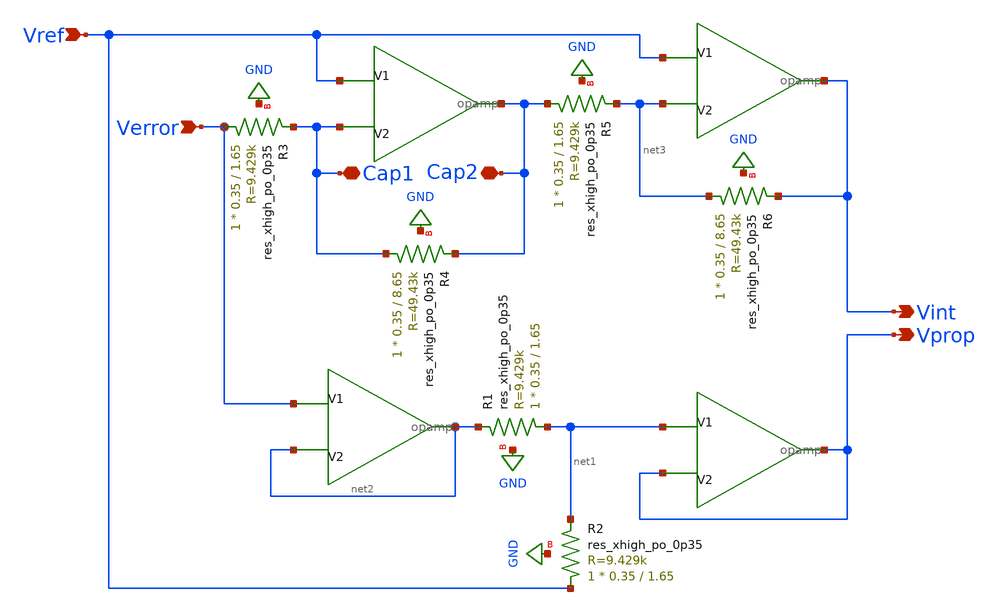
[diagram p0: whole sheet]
** sch_path: schematics/PI_controller.sch
**.subckt PI_controller Verror Vref Cap1 Cap2 Vint Vprop
*.ipin Verror
*.ipin Vref
*.iopin Cap1
*.iopin Cap2
*.opin Vint
*.opin Vprop
X3 Verror net2 net2 opamp
XR1 net1 net2 GND sky130_fd_pr__res_xhigh_po_0p35 L=1.65 mult=1 m=1
X1 net1 Vprop Vprop opamp
XR2 Vref net1 GND sky130_fd_pr__res_xhigh_po_0p35 L=1.65 mult=1 m=1
X2 Vref Cap1 Cap2 opamp
X4 Vref net3 Vint opamp
XR3 Verror Cap1 GND sky130_fd_pr__res_xhigh_po_0p35 L=1.65 mult=1 m=1
XR4 Cap1 Cap2 GND sky130_fd_pr__res_xhigh_po_0p35 L=8.65 mult=1 m=1
XR5 Cap2 net3 GND sky130_fd_pr__res_xhigh_po_0p35 L=1.65 mult=1 m=1
XR6 net3 Vint GND sky130_fd_pr__res_xhigh_po_0p35 L=8.65 mult=1 m=1
**.ends

* expanding   symbol:  /home/madvlsi/Documents/MADVLSI_final/schematics/opamp.sym # of pins=3
** sym_path: schematics/opamp.sym
** sch_path: schematics/opamp.sch
.subckt opamp V1 V2 VOUT
*.ipin V1
*.ipin V2
*.opin VOUT
XM19 net12 net10 GND VDD sky130_fd_pr__pfet_01v8 L=.6 W=1.5 nf=1 ad='int((nf+1)/2) * W/nf * 0.29' as='int((nf+2)/2) * W/nf * 0.29'
+ pd='2*int((nf+1)/2) * (W/nf + 0.29)' ps='2*int((nf+2)/2) * (W/nf + 0.29)' nrd='0.29 / W' nrs='0.29 / W'
+ sa=0 sb=0 sd=0 mult=1 m=1
XMD20 VDD VDD net12 VDD sky130_fd_pr__pfet_01v8 L=.6 W=1.5 nf=1 ad='int((nf+1)/2) * W/nf * 0.29' as='int((nf+2)/2) * W/nf * 0.29'
+ pd='2*int((nf+1)/2) * (W/nf + 0.29)' ps='2*int((nf+2)/2) * (W/nf + 0.29)' nrd='0.29 / W' nrs='0.29 / W'
+ sa=0 sb=0 sd=0 mult=1 m=1
XM22 net12 net10 net9 VDD sky130_fd_pr__pfet_01v8 L=.6 W=1.5 nf=1 ad='int((nf+1)/2) * W/nf * 0.29' as='int((nf+2)/2) * W/nf * 0.29'
+ pd='2*int((nf+1)/2) * (W/nf + 0.29)' ps='2*int((nf+2)/2) * (W/nf + 0.29)' nrd='0.29 / W' nrs='0.29 / W'
+ sa=0 sb=0 sd=0 mult=1 m=1
XM23 GND net10 net12 VDD sky130_fd_pr__pfet_01v8 L=.6 W=1.5 nf=1 ad='int((nf+1)/2) * W/nf * 0.29' as='int((nf+2)/2) * W/nf * 0.29'
+ pd='2*int((nf+1)/2) * (W/nf + 0.29)' ps='2*int((nf+2)/2) * (W/nf + 0.29)' nrd='0.29 / W' nrs='0.29 / W'
+ sa=0 sb=0 sd=0 mult=1 m=1
XMD24 net9 VDD net10 VDD sky130_fd_pr__pfet_01v8 L=.6 W=1.5 nf=1 ad='int((nf+1)/2) * W/nf * 0.29' as='int((nf+2)/2) * W/nf * 0.29'
+ pd='2*int((nf+1)/2) * (W/nf + 0.29)' ps='2*int((nf+2)/2) * (W/nf + 0.29)' nrd='0.29 / W' nrs='0.29 / W'
+ sa=0 sb=0 sd=0 mult=1 m=1
XM25 VDD net10 net12 VDD sky130_fd_pr__pfet_01v8 L=.6 W=1.5 nf=1 ad='int((nf+1)/2) * W/nf * 0.29' as='int((nf+2)/2) * W/nf * 0.29'
+ pd='2*int((nf+1)/2) * (W/nf + 0.29)' ps='2*int((nf+2)/2) * (W/nf + 0.29)' nrd='0.29 / W' nrs='0.29 / W'
+ sa=0 sb=0 sd=0 mult=1 m=1
XM26 net7 V2 net11 VDD sky130_fd_pr__pfet_01v8 L=.6 W=1.5 nf=1 ad='int((nf+1)/2) * W/nf * 0.29' as='int((nf+2)/2) * W/nf * 0.29'
+ pd='2*int((nf+1)/2) * (W/nf + 0.29)' ps='2*int((nf+2)/2) * (W/nf + 0.29)' nrd='0.29 / W' nrs='0.29 / W'
+ sa=0 sb=0 sd=0 mult=1 m=1
XMD27 net5 VDD net14 VDD sky130_fd_pr__pfet_01v8 L=.6 W=1.5 nf=1 ad='int((nf+1)/2) * W/nf * 0.29' as='int((nf+2)/2) * W/nf * 0.29'
+ pd='2*int((nf+1)/2) * (W/nf + 0.29)' ps='2*int((nf+2)/2) * (W/nf + 0.29)' nrd='0.29 / W' nrs='0.29 / W'
+ sa=0 sb=0 sd=0 mult=1 m=1
XM28 net6 V1 net11 VDD sky130_fd_pr__pfet_01v8 L=.6 W=1.5 nf=1 ad='int((nf+1)/2) * W/nf * 0.29' as='int((nf+2)/2) * W/nf * 0.29'
+ pd='2*int((nf+1)/2) * (W/nf + 0.29)' ps='2*int((nf+2)/2) * (W/nf + 0.29)' nrd='0.29 / W' nrs='0.29 / W'
+ sa=0 sb=0 sd=0 mult=1 m=1
XM29 net11 net10 VDD VDD sky130_fd_pr__pfet_01v8 L=.6 W=1.5 nf=1 ad='int((nf+1)/2) * W/nf * 0.29' as='int((nf+2)/2) * W/nf * 0.29'
+ pd='2*int((nf+1)/2) * (W/nf + 0.29)' ps='2*int((nf+2)/2) * (W/nf + 0.29)' nrd='0.29 / W' nrs='0.29 / W'
+ sa=0 sb=0 sd=0 mult=1 m=1
XMD30 net11 VDD VDD VDD sky130_fd_pr__pfet_01v8 L=.6 W=1.5 nf=1 ad='int((nf+1)/2) * W/nf * 0.29' as='int((nf+2)/2) * W/nf * 0.29'
+ pd='2*int((nf+1)/2) * (W/nf + 0.29)' ps='2*int((nf+2)/2) * (W/nf + 0.29)' nrd='0.29 / W' nrs='0.29 / W'
+ sa=0 sb=0 sd=0 mult=1 m=1
XMD31 net2 VDD net13 VDD sky130_fd_pr__pfet_01v8 L=.6 W=1.5 nf=1 ad='int((nf+1)/2) * W/nf * 0.29' as='int((nf+2)/2) * W/nf * 0.29'
+ pd='2*int((nf+1)/2) * (W/nf + 0.29)' ps='2*int((nf+2)/2) * (W/nf + 0.29)' nrd='0.29 / W' nrs='0.29 / W'
+ sa=0 sb=0 sd=0 mult=1 m=1
XM32 net4 net5 net5 VDD sky130_fd_pr__pfet_01v8 L=.6 W=1.5 nf=1 ad='int((nf+1)/2) * W/nf * 0.29' as='int((nf+2)/2) * W/nf * 0.29'
+ pd='2*int((nf+1)/2) * (W/nf + 0.29)' ps='2*int((nf+2)/2) * (W/nf + 0.29)' nrd='0.29 / W' nrs='0.29 / W'
+ sa=0 sb=0 sd=0 mult=1 m=1
XM33 VDD net10 net4 VDD sky130_fd_pr__pfet_01v8 L=.6 W=1.5 nf=1 ad='int((nf+1)/2) * W/nf * 0.29' as='int((nf+2)/2) * W/nf * 0.29'
+ pd='2*int((nf+1)/2) * (W/nf + 0.29)' ps='2*int((nf+2)/2) * (W/nf + 0.29)' nrd='0.29 / W' nrs='0.29 / W'
+ sa=0 sb=0 sd=0 mult=1 m=1
XM34 net3 net5 net2 VDD sky130_fd_pr__pfet_01v8 L=.6 W=1.5 nf=1 ad='int((nf+1)/2) * W/nf * 0.29' as='int((nf+2)/2) * W/nf * 0.29'
+ pd='2*int((nf+1)/2) * (W/nf + 0.29)' ps='2*int((nf+2)/2) * (W/nf + 0.29)' nrd='0.29 / W' nrs='0.29 / W'
+ sa=0 sb=0 sd=0 mult=1 m=1
XM35 VDD net10 net3 VDD sky130_fd_pr__pfet_01v8 L=.6 W=1.5 nf=1 ad='int((nf+1)/2) * W/nf * 0.29' as='int((nf+2)/2) * W/nf * 0.29'
+ pd='2*int((nf+1)/2) * (W/nf + 0.29)' ps='2*int((nf+2)/2) * (W/nf + 0.29)' nrd='0.29 / W' nrs='0.29 / W'
+ sa=0 sb=0 sd=0 mult=1 m=1
XM36 VOUT net2 VDD VDD sky130_fd_pr__pfet_01v8 L=.6 W=1.5 nf=1 ad='int((nf+1)/2) * W/nf * 0.29' as='int((nf+2)/2) * W/nf * 0.29'
+ pd='2*int((nf+1)/2) * (W/nf + 0.29)' ps='2*int((nf+2)/2) * (W/nf + 0.29)' nrd='0.29 / W' nrs='0.29 / W'
+ sa=0 sb=0 sd=0 mult=1 m=1
XM37 VDD net2 VOUT VDD sky130_fd_pr__pfet_01v8 L=.6 W=1.5 nf=1 ad='int((nf+1)/2) * W/nf * 0.29' as='int((nf+2)/2) * W/nf * 0.29'
+ pd='2*int((nf+1)/2) * (W/nf + 0.29)' ps='2*int((nf+2)/2) * (W/nf + 0.29)' nrd='0.29 / W' nrs='0.29 / W'
+ sa=0 sb=0 sd=0 mult=1 m=1
XM38 VOUT net2 VDD VDD sky130_fd_pr__pfet_01v8 L=.6 W=1.5 nf=1 ad='int((nf+1)/2) * W/nf * 0.29' as='int((nf+2)/2) * W/nf * 0.29'
+ pd='2*int((nf+1)/2) * (W/nf + 0.29)' ps='2*int((nf+2)/2) * (W/nf + 0.29)' nrd='0.29 / W' nrs='0.29 / W'
+ sa=0 sb=0 sd=0 mult=1 m=1
XM39 VDD net2 VOUT VDD sky130_fd_pr__pfet_01v8 L=.6 W=1.5 nf=1 ad='int((nf+1)/2) * W/nf * 0.29' as='int((nf+2)/2) * W/nf * 0.29'
+ pd='2*int((nf+1)/2) * (W/nf + 0.29)' ps='2*int((nf+2)/2) * (W/nf + 0.29)' nrd='0.29 / W' nrs='0.29 / W'
+ sa=0 sb=0 sd=0 mult=1 m=1
XM40 net1 net9 VDD GND sky130_fd_pr__nfet_01v8 L=.6 W=1.5 nf=1 ad='int((nf+1)/2) * W/nf * 0.29' as='int((nf+2)/2) * W/nf * 0.29'
+ pd='2*int((nf+1)/2) * (W/nf + 0.29)' ps='2*int((nf+2)/2) * (W/nf + 0.29)' nrd='0.29 / W' nrs='0.29 / W'
+ sa=0 sb=0 sd=0 mult=1 m=1
XMD41 GND GND net1 GND sky130_fd_pr__nfet_01v8 L=.6 W=1.5 nf=1 ad='int((nf+1)/2) * W/nf * 0.29' as='int((nf+2)/2) * W/nf * 0.29'
+ pd='2*int((nf+1)/2) * (W/nf + 0.29)' ps='2*int((nf+2)/2) * (W/nf + 0.29)' nrd='0.29 / W' nrs='0.29 / W'
+ sa=0 sb=0 sd=0 mult=1 m=1
XM42 net1 net9 net10 GND sky130_fd_pr__nfet_01v8 L=.6 W=1.5 nf=1 ad='int((nf+1)/2) * W/nf * 0.29' as='int((nf+2)/2) * W/nf * 0.29'
+ pd='2*int((nf+1)/2) * (W/nf + 0.29)' ps='2*int((nf+2)/2) * (W/nf + 0.29)' nrd='0.29 / W' nrs='0.29 / W'
+ sa=0 sb=0 sd=0 mult=1 m=1
XM43 VDD net9 net1 GND sky130_fd_pr__nfet_01v8 L=.6 W=1.5 nf=1 ad='int((nf+1)/2) * W/nf * 0.29' as='int((nf+2)/2) * W/nf * 0.29'
+ pd='2*int((nf+1)/2) * (W/nf + 0.29)' ps='2*int((nf+2)/2) * (W/nf + 0.29)' nrd='0.29 / W' nrs='0.29 / W'
+ sa=0 sb=0 sd=0 mult=1 m=1
XMD44 net10 GND net9 GND sky130_fd_pr__nfet_01v8 L=.6 W=1.5 nf=1 ad='int((nf+1)/2) * W/nf * 0.29' as='int((nf+2)/2) * W/nf * 0.29'
+ pd='2*int((nf+1)/2) * (W/nf + 0.29)' ps='2*int((nf+2)/2) * (W/nf + 0.29)' nrd='0.29 / W' nrs='0.29 / W'
+ sa=0 sb=0 sd=0 mult=1 m=1
XM45 GND net9 net1 GND sky130_fd_pr__nfet_01v8 L=.6 W=1.5 nf=1 ad='int((nf+1)/2) * W/nf * 0.29' as='int((nf+2)/2) * W/nf * 0.29'
+ pd='2*int((nf+1)/2) * (W/nf + 0.29)' ps='2*int((nf+2)/2) * (W/nf + 0.29)' nrd='0.29 / W' nrs='0.29 / W'
+ sa=0 sb=0 sd=0 mult=1 m=1
XM46 net3 V1 net8 GND sky130_fd_pr__nfet_01v8 L=.6 W=1.5 nf=1 ad='int((nf+1)/2) * W/nf * 0.29' as='int((nf+2)/2) * W/nf * 0.29'
+ pd='2*int((nf+1)/2) * (W/nf + 0.29)' ps='2*int((nf+2)/2) * (W/nf + 0.29)' nrd='0.29 / W' nrs='0.29 / W'
+ sa=0 sb=0 sd=0 mult=1 m=1
XMD47 net5 GND net15 GND sky130_fd_pr__nfet_01v8 L=.6 W=1.5 nf=1 ad='int((nf+1)/2) * W/nf * 0.29' as='int((nf+2)/2) * W/nf * 0.29'
+ pd='2*int((nf+1)/2) * (W/nf + 0.29)' ps='2*int((nf+2)/2) * (W/nf + 0.29)' nrd='0.29 / W' nrs='0.29 / W'
+ sa=0 sb=0 sd=0 mult=1 m=1
XM48 net4 V2 net8 GND sky130_fd_pr__nfet_01v8 L=.6 W=1.5 nf=1 ad='int((nf+1)/2) * W/nf * 0.29' as='int((nf+2)/2) * W/nf * 0.29'
+ pd='2*int((nf+1)/2) * (W/nf + 0.29)' ps='2*int((nf+2)/2) * (W/nf + 0.29)' nrd='0.29 / W' nrs='0.29 / W'
+ sa=0 sb=0 sd=0 mult=1 m=1
XM49 net8 net9 GND GND sky130_fd_pr__nfet_01v8 L=.6 W=1.5 nf=1 ad='int((nf+1)/2) * W/nf * 0.29' as='int((nf+2)/2) * W/nf * 0.29'
+ pd='2*int((nf+1)/2) * (W/nf + 0.29)' ps='2*int((nf+2)/2) * (W/nf + 0.29)' nrd='0.29 / W' nrs='0.29 / W'
+ sa=0 sb=0 sd=0 mult=1 m=1
XMD50 net8 GND GND GND sky130_fd_pr__nfet_01v8 L=.6 W=1.5 nf=1 ad='int((nf+1)/2) * W/nf * 0.29' as='int((nf+2)/2) * W/nf * 0.29'
+ pd='2*int((nf+1)/2) * (W/nf + 0.29)' ps='2*int((nf+2)/2) * (W/nf + 0.29)' nrd='0.29 / W' nrs='0.29 / W'
+ sa=0 sb=0 sd=0 mult=1 m=1
XMD51 net2 GND net16 GND sky130_fd_pr__nfet_01v8 L=.6 W=1.5 nf=1 ad='int((nf+1)/2) * W/nf * 0.29' as='int((nf+2)/2) * W/nf * 0.29'
+ pd='2*int((nf+1)/2) * (W/nf + 0.29)' ps='2*int((nf+2)/2) * (W/nf + 0.29)' nrd='0.29 / W' nrs='0.29 / W'
+ sa=0 sb=0 sd=0 mult=1 m=1
XM52 GND net9 net7 GND sky130_fd_pr__nfet_01v8 L=.6 W=1.5 nf=1 ad='int((nf+1)/2) * W/nf * 0.29' as='int((nf+2)/2) * W/nf * 0.29'
+ pd='2*int((nf+1)/2) * (W/nf + 0.29)' ps='2*int((nf+2)/2) * (W/nf + 0.29)' nrd='0.29 / W' nrs='0.29 / W'
+ sa=0 sb=0 sd=0 mult=1 m=1
XMD53 VOUT GND GND GND sky130_fd_pr__nfet_01v8 L=.6 W=1.5 nf=1 ad='int((nf+1)/2) * W/nf * 0.29' as='int((nf+2)/2) * W/nf * 0.29'
+ pd='2*int((nf+1)/2) * (W/nf + 0.29)' ps='2*int((nf+2)/2) * (W/nf + 0.29)' nrd='0.29 / W' nrs='0.29 / W'
+ sa=0 sb=0 sd=0 mult=1 m=1
XM54 GND net9 net6 GND sky130_fd_pr__nfet_01v8 L=.6 W=1.5 nf=1 ad='int((nf+1)/2) * W/nf * 0.29' as='int((nf+2)/2) * W/nf * 0.29'
+ pd='2*int((nf+1)/2) * (W/nf + 0.29)' ps='2*int((nf+2)/2) * (W/nf + 0.29)' nrd='0.29 / W' nrs='0.29 / W'
+ sa=0 sb=0 sd=0 mult=1 m=1
XM55 net7 net5 net5 GND sky130_fd_pr__nfet_01v8 L=.6 W=1.5 nf=1 ad='int((nf+1)/2) * W/nf * 0.29' as='int((nf+2)/2) * W/nf * 0.29'
+ pd='2*int((nf+1)/2) * (W/nf + 0.29)' ps='2*int((nf+2)/2) * (W/nf + 0.29)' nrd='0.29 / W' nrs='0.29 / W'
+ sa=0 sb=0 sd=0 mult=1 m=1
XM56 net6 net5 net2 GND sky130_fd_pr__nfet_01v8 L=.6 W=1.5 nf=1 ad='int((nf+1)/2) * W/nf * 0.29' as='int((nf+2)/2) * W/nf * 0.29'
+ pd='2*int((nf+1)/2) * (W/nf + 0.29)' ps='2*int((nf+2)/2) * (W/nf + 0.29)' nrd='0.29 / W' nrs='0.29 / W'
+ sa=0 sb=0 sd=0 mult=1 m=1
XMD57 VOUT GND GND GND sky130_fd_pr__nfet_01v8 L=.6 W=1.5 nf=1 ad='int((nf+1)/2) * W/nf * 0.29' as='int((nf+2)/2) * W/nf * 0.29'
+ pd='2*int((nf+1)/2) * (W/nf + 0.29)' ps='2*int((nf+2)/2) * (W/nf + 0.29)' nrd='0.29 / W' nrs='0.29 / W'
+ sa=0 sb=0 sd=0 mult=1 m=1
XM58 GND net2 VOUT GND sky130_fd_pr__nfet_01v8 L=.6 W=1.5 nf=1 ad='int((nf+1)/2) * W/nf * 0.29' as='int((nf+2)/2) * W/nf * 0.29'
+ pd='2*int((nf+1)/2) * (W/nf + 0.29)' ps='2*int((nf+2)/2) * (W/nf + 0.29)' nrd='0.29 / W' nrs='0.29 / W'
+ sa=0 sb=0 sd=0 mult=1 m=1
XM59 GND net2 VOUT GND sky130_fd_pr__nfet_01v8 L=.6 W=1.5 nf=1 ad='int((nf+1)/2) * W/nf * 0.29' as='int((nf+2)/2) * W/nf * 0.29'
+ pd='2*int((nf+1)/2) * (W/nf + 0.29)' ps='2*int((nf+2)/2) * (W/nf + 0.29)' nrd='0.29 / W' nrs='0.29 / W'
+ sa=0 sb=0 sd=0 mult=1 m=1
XM60 net12 net10 GND VDD sky130_fd_pr__pfet_01v8 L=.6 W=1.5 nf=1 ad='int((nf+1)/2) * W/nf * 0.29' as='int((nf+2)/2) * W/nf * 0.29'
+ pd='2*int((nf+1)/2) * (W/nf + 0.29)' ps='2*int((nf+2)/2) * (W/nf + 0.29)' nrd='0.29 / W' nrs='0.29 / W'
+ sa=0 sb=0 sd=0 mult=1 m=1
XM61 net10 net10 net4 VDD sky130_fd_pr__pfet_01v8 L=.6 W=1.5 nf=1 ad='int((nf+1)/2) * W/nf * 0.29' as='int((nf+2)/2) * W/nf * 0.29'
+ pd='2*int((nf+1)/2) * (W/nf + 0.29)' ps='2*int((nf+2)/2) * (W/nf + 0.29)' nrd='0.29 / W' nrs='0.29 / W'
+ sa=0 sb=0 sd=0 mult=1 m=1
XM62 net1 net9 VDD GND sky130_fd_pr__nfet_01v8 L=.6 W=1.5 nf=1 ad='int((nf+1)/2) * W/nf * 0.29' as='int((nf+2)/2) * W/nf * 0.29'
+ pd='2*int((nf+1)/2) * (W/nf + 0.29)' ps='2*int((nf+2)/2) * (W/nf + 0.29)' nrd='0.29 / W' nrs='0.29 / W'
+ sa=0 sb=0 sd=0 mult=1 m=1
XM63 net9 net9 net7 GND sky130_fd_pr__nfet_01v8 L=.6 W=1.5 nf=1 ad='int((nf+1)/2) * W/nf * 0.29' as='int((nf+2)/2) * W/nf * 0.29'
+ pd='2*int((nf+1)/2) * (W/nf + 0.29)' ps='2*int((nf+2)/2) * (W/nf + 0.29)' nrd='0.29 / W' nrs='0.29 / W'
+ sa=0 sb=0 sd=0 mult=1 m=1
XMD64 VDD GND GND GND sky130_fd_pr__nfet_01v8 L=.6 W=1.5 nf=1 ad='int((nf+1)/2) * W/nf * 0.29' as='int((nf+2)/2) * W/nf * 0.29'
+ pd='2*int((nf+1)/2) * (W/nf + 0.29)' ps='2*int((nf+2)/2) * (W/nf + 0.29)' nrd='0.29 / W' nrs='0.29 / W'
+ sa=0 sb=0 sd=0 mult=1 m=1
XMD65 net7 GND GND GND sky130_fd_pr__nfet_01v8 L=.6 W=1.5 nf=1 ad='int((nf+1)/2) * W/nf * 0.29' as='int((nf+2)/2) * W/nf * 0.29'
+ pd='2*int((nf+1)/2) * (W/nf + 0.29)' ps='2*int((nf+2)/2) * (W/nf + 0.29)' nrd='0.29 / W' nrs='0.29 / W'
+ sa=0 sb=0 sd=0 mult=1 m=1
XMD66 GND VDD VDD VDD sky130_fd_pr__pfet_01v8 L=.6 W=1.5 nf=1 ad='int((nf+1)/2) * W/nf * 0.29' as='int((nf+2)/2) * W/nf * 0.29'
+ pd='2*int((nf+1)/2) * (W/nf + 0.29)' ps='2*int((nf+2)/2) * (W/nf + 0.29)' nrd='0.29 / W' nrs='0.29 / W'
+ sa=0 sb=0 sd=0 mult=1 m=1
XMD67 net4 VDD VDD VDD sky130_fd_pr__pfet_01v8 L=.6 W=1.5 nf=1 ad='int((nf+1)/2) * W/nf * 0.29' as='int((nf+2)/2) * W/nf * 0.29'
+ pd='2*int((nf+1)/2) * (W/nf + 0.29)' ps='2*int((nf+2)/2) * (W/nf + 0.29)' nrd='0.29 / W' nrs='0.29 / W'
+ sa=0 sb=0 sd=0 mult=1 m=1
XMD1 net15 GND net3 GND sky130_fd_pr__nfet_01v8 L=.6 W=1.5 nf=1 ad='int((nf+1)/2) * W/nf * 0.29' as='int((nf+2)/2) * W/nf * 0.29'
+ pd='2*int((nf+1)/2) * (W/nf + 0.29)' ps='2*int((nf+2)/2) * (W/nf + 0.29)' nrd='0.29 / W' nrs='0.29 / W'
+ sa=0 sb=0 sd=0 mult=1 m=1
XMD2 net16 GND net4 GND sky130_fd_pr__nfet_01v8 L=.6 W=1.5 nf=1 ad='int((nf+1)/2) * W/nf * 0.29' as='int((nf+2)/2) * W/nf * 0.29'
+ pd='2*int((nf+1)/2) * (W/nf + 0.29)' ps='2*int((nf+2)/2) * (W/nf + 0.29)' nrd='0.29 / W' nrs='0.29 / W'
+ sa=0 sb=0 sd=0 mult=1 m=1
XMD3 net13 VDD net6 VDD sky130_fd_pr__pfet_01v8 L=.6 W=1.5 nf=1 ad='int((nf+1)/2) * W/nf * 0.29' as='int((nf+2)/2) * W/nf * 0.29'
+ pd='2*int((nf+1)/2) * (W/nf + 0.29)' ps='2*int((nf+2)/2) * (W/nf + 0.29)' nrd='0.29 / W' nrs='0.29 / W'
+ sa=0 sb=0 sd=0 mult=1 m=1
XMD4 net14 VDD net7 VDD sky130_fd_pr__pfet_01v8 L=.6 W=1.5 nf=1 ad='int((nf+1)/2) * W/nf * 0.29' as='int((nf+2)/2) * W/nf * 0.29'
+ pd='2*int((nf+1)/2) * (W/nf + 0.29)' ps='2*int((nf+2)/2) * (W/nf + 0.29)' nrd='0.29 / W' nrs='0.29 / W'
+ sa=0 sb=0 sd=0 mult=1 m=1
XM1 net21 net10 GND VDD sky130_fd_pr__pfet_01v8 L=.6 W=1.5 nf=1 ad='int((nf+1)/2) * W/nf * 0.29' as='int((nf+2)/2) * W/nf * 0.29'
+ pd='2*int((nf+1)/2) * (W/nf + 0.29)' ps='2*int((nf+2)/2) * (W/nf + 0.29)' nrd='0.29 / W' nrs='0.29 / W'
+ sa=0 sb=0 sd=0 mult=1 m=1
XMD5 VDD VDD net21 VDD sky130_fd_pr__pfet_01v8 L=.6 W=1.5 nf=1 ad='int((nf+1)/2) * W/nf * 0.29' as='int((nf+2)/2) * W/nf * 0.29'
+ pd='2*int((nf+1)/2) * (W/nf + 0.29)' ps='2*int((nf+2)/2) * (W/nf + 0.29)' nrd='0.29 / W' nrs='0.29 / W'
+ sa=0 sb=0 sd=0 mult=1 m=1
XM6 net21 net10 net9 VDD sky130_fd_pr__pfet_01v8 L=.6 W=1.5 nf=1 ad='int((nf+1)/2) * W/nf * 0.29' as='int((nf+2)/2) * W/nf * 0.29'
+ pd='2*int((nf+1)/2) * (W/nf + 0.29)' ps='2*int((nf+2)/2) * (W/nf + 0.29)' nrd='0.29 / W' nrs='0.29 / W'
+ sa=0 sb=0 sd=0 mult=1 m=1
XM7 GND net10 net21 VDD sky130_fd_pr__pfet_01v8 L=.6 W=1.5 nf=1 ad='int((nf+1)/2) * W/nf * 0.29' as='int((nf+2)/2) * W/nf * 0.29'
+ pd='2*int((nf+1)/2) * (W/nf + 0.29)' ps='2*int((nf+2)/2) * (W/nf + 0.29)' nrd='0.29 / W' nrs='0.29 / W'
+ sa=0 sb=0 sd=0 mult=1 m=1
XMD8 net9 VDD net10 VDD sky130_fd_pr__pfet_01v8 L=.6 W=1.5 nf=1 ad='int((nf+1)/2) * W/nf * 0.29' as='int((nf+2)/2) * W/nf * 0.29'
+ pd='2*int((nf+1)/2) * (W/nf + 0.29)' ps='2*int((nf+2)/2) * (W/nf + 0.29)' nrd='0.29 / W' nrs='0.29 / W'
+ sa=0 sb=0 sd=0 mult=1 m=1
XM9 VDD net10 net21 VDD sky130_fd_pr__pfet_01v8 L=.6 W=1.5 nf=1 ad='int((nf+1)/2) * W/nf * 0.29' as='int((nf+2)/2) * W/nf * 0.29'
+ pd='2*int((nf+1)/2) * (W/nf + 0.29)' ps='2*int((nf+2)/2) * (W/nf + 0.29)' nrd='0.29 / W' nrs='0.29 / W'
+ sa=0 sb=0 sd=0 mult=1 m=1
XM10 net7 V2 net20 VDD sky130_fd_pr__pfet_01v8 L=.6 W=1.5 nf=1 ad='int((nf+1)/2) * W/nf * 0.29' as='int((nf+2)/2) * W/nf * 0.29'
+ pd='2*int((nf+1)/2) * (W/nf + 0.29)' ps='2*int((nf+2)/2) * (W/nf + 0.29)' nrd='0.29 / W' nrs='0.29 / W'
+ sa=0 sb=0 sd=0 mult=1 m=1
XMD11 net18 VDD net23 VDD sky130_fd_pr__pfet_01v8 L=.6 W=1.5 nf=1 ad='int((nf+1)/2) * W/nf * 0.29' as='int((nf+2)/2) * W/nf * 0.29'
+ pd='2*int((nf+1)/2) * (W/nf + 0.29)' ps='2*int((nf+2)/2) * (W/nf + 0.29)' nrd='0.29 / W' nrs='0.29 / W'
+ sa=0 sb=0 sd=0 mult=1 m=1
XM12 net6 V1 net20 VDD sky130_fd_pr__pfet_01v8 L=.6 W=1.5 nf=1 ad='int((nf+1)/2) * W/nf * 0.29' as='int((nf+2)/2) * W/nf * 0.29'
+ pd='2*int((nf+1)/2) * (W/nf + 0.29)' ps='2*int((nf+2)/2) * (W/nf + 0.29)' nrd='0.29 / W' nrs='0.29 / W'
+ sa=0 sb=0 sd=0 mult=1 m=1
XM13 net20 net10 VDD VDD sky130_fd_pr__pfet_01v8 L=.6 W=1.5 nf=1 ad='int((nf+1)/2) * W/nf * 0.29' as='int((nf+2)/2) * W/nf * 0.29'
+ pd='2*int((nf+1)/2) * (W/nf + 0.29)' ps='2*int((nf+2)/2) * (W/nf + 0.29)' nrd='0.29 / W' nrs='0.29 / W'
+ sa=0 sb=0 sd=0 mult=1 m=1
XMD14 net20 VDD VDD VDD sky130_fd_pr__pfet_01v8 L=.6 W=1.5 nf=1 ad='int((nf+1)/2) * W/nf * 0.29' as='int((nf+2)/2) * W/nf * 0.29'
+ pd='2*int((nf+1)/2) * (W/nf + 0.29)' ps='2*int((nf+2)/2) * (W/nf + 0.29)' nrd='0.29 / W' nrs='0.29 / W'
+ sa=0 sb=0 sd=0 mult=1 m=1
XMD15 net2 VDD net22 VDD sky130_fd_pr__pfet_01v8 L=.6 W=1.5 nf=1 ad='int((nf+1)/2) * W/nf * 0.29' as='int((nf+2)/2) * W/nf * 0.29'
+ pd='2*int((nf+1)/2) * (W/nf + 0.29)' ps='2*int((nf+2)/2) * (W/nf + 0.29)' nrd='0.29 / W' nrs='0.29 / W'
+ sa=0 sb=0 sd=0 mult=1 m=1
XM16 net4 net18 net18 VDD sky130_fd_pr__pfet_01v8 L=.6 W=1.5 nf=1 ad='int((nf+1)/2) * W/nf * 0.29' as='int((nf+2)/2) * W/nf * 0.29'
+ pd='2*int((nf+1)/2) * (W/nf + 0.29)' ps='2*int((nf+2)/2) * (W/nf + 0.29)' nrd='0.29 / W' nrs='0.29 / W'
+ sa=0 sb=0 sd=0 mult=1 m=1
XM17 VDD net10 net4 VDD sky130_fd_pr__pfet_01v8 L=.6 W=1.5 nf=1 ad='int((nf+1)/2) * W/nf * 0.29' as='int((nf+2)/2) * W/nf * 0.29'
+ pd='2*int((nf+1)/2) * (W/nf + 0.29)' ps='2*int((nf+2)/2) * (W/nf + 0.29)' nrd='0.29 / W' nrs='0.29 / W'
+ sa=0 sb=0 sd=0 mult=1 m=1
XM18 net3 net18 net2 VDD sky130_fd_pr__pfet_01v8 L=.6 W=1.5 nf=1 ad='int((nf+1)/2) * W/nf * 0.29' as='int((nf+2)/2) * W/nf * 0.29'
+ pd='2*int((nf+1)/2) * (W/nf + 0.29)' ps='2*int((nf+2)/2) * (W/nf + 0.29)' nrd='0.29 / W' nrs='0.29 / W'
+ sa=0 sb=0 sd=0 mult=1 m=1
XM20 VDD net10 net3 VDD sky130_fd_pr__pfet_01v8 L=.6 W=1.5 nf=1 ad='int((nf+1)/2) * W/nf * 0.29' as='int((nf+2)/2) * W/nf * 0.29'
+ pd='2*int((nf+1)/2) * (W/nf + 0.29)' ps='2*int((nf+2)/2) * (W/nf + 0.29)' nrd='0.29 / W' nrs='0.29 / W'
+ sa=0 sb=0 sd=0 mult=1 m=1
XM21 VOUT net2 VDD VDD sky130_fd_pr__pfet_01v8 L=.6 W=1.5 nf=1 ad='int((nf+1)/2) * W/nf * 0.29' as='int((nf+2)/2) * W/nf * 0.29'
+ pd='2*int((nf+1)/2) * (W/nf + 0.29)' ps='2*int((nf+2)/2) * (W/nf + 0.29)' nrd='0.29 / W' nrs='0.29 / W'
+ sa=0 sb=0 sd=0 mult=1 m=1
XM24 VDD net2 VOUT VDD sky130_fd_pr__pfet_01v8 L=.6 W=1.5 nf=1 ad='int((nf+1)/2) * W/nf * 0.29' as='int((nf+2)/2) * W/nf * 0.29'
+ pd='2*int((nf+1)/2) * (W/nf + 0.29)' ps='2*int((nf+2)/2) * (W/nf + 0.29)' nrd='0.29 / W' nrs='0.29 / W'
+ sa=0 sb=0 sd=0 mult=1 m=1
XM27 VOUT net2 VDD VDD sky130_fd_pr__pfet_01v8 L=.6 W=1.5 nf=1 ad='int((nf+1)/2) * W/nf * 0.29' as='int((nf+2)/2) * W/nf * 0.29'
+ pd='2*int((nf+1)/2) * (W/nf + 0.29)' ps='2*int((nf+2)/2) * (W/nf + 0.29)' nrd='0.29 / W' nrs='0.29 / W'
+ sa=0 sb=0 sd=0 mult=1 m=1
XM30 VDD net2 VOUT VDD sky130_fd_pr__pfet_01v8 L=.6 W=1.5 nf=1 ad='int((nf+1)/2) * W/nf * 0.29' as='int((nf+2)/2) * W/nf * 0.29'
+ pd='2*int((nf+1)/2) * (W/nf + 0.29)' ps='2*int((nf+2)/2) * (W/nf + 0.29)' nrd='0.29 / W' nrs='0.29 / W'
+ sa=0 sb=0 sd=0 mult=1 m=1
XM31 net17 net9 VDD GND sky130_fd_pr__nfet_01v8 L=.6 W=1.5 nf=1 ad='int((nf+1)/2) * W/nf * 0.29' as='int((nf+2)/2) * W/nf * 0.29'
+ pd='2*int((nf+1)/2) * (W/nf + 0.29)' ps='2*int((nf+2)/2) * (W/nf + 0.29)' nrd='0.29 / W' nrs='0.29 / W'
+ sa=0 sb=0 sd=0 mult=1 m=1
XMD32 GND GND net17 GND sky130_fd_pr__nfet_01v8 L=.6 W=1.5 nf=1 ad='int((nf+1)/2) * W/nf * 0.29' as='int((nf+2)/2) * W/nf * 0.29'
+ pd='2*int((nf+1)/2) * (W/nf + 0.29)' ps='2*int((nf+2)/2) * (W/nf + 0.29)' nrd='0.29 / W' nrs='0.29 / W'
+ sa=0 sb=0 sd=0 mult=1 m=1
XM41 net17 net9 net10 GND sky130_fd_pr__nfet_01v8 L=.6 W=1.5 nf=1 ad='int((nf+1)/2) * W/nf * 0.29' as='int((nf+2)/2) * W/nf * 0.29'
+ pd='2*int((nf+1)/2) * (W/nf + 0.29)' ps='2*int((nf+2)/2) * (W/nf + 0.29)' nrd='0.29 / W' nrs='0.29 / W'
+ sa=0 sb=0 sd=0 mult=1 m=1
XM44 VDD net9 net17 GND sky130_fd_pr__nfet_01v8 L=.6 W=1.5 nf=1 ad='int((nf+1)/2) * W/nf * 0.29' as='int((nf+2)/2) * W/nf * 0.29'
+ pd='2*int((nf+1)/2) * (W/nf + 0.29)' ps='2*int((nf+2)/2) * (W/nf + 0.29)' nrd='0.29 / W' nrs='0.29 / W'
+ sa=0 sb=0 sd=0 mult=1 m=1
XMD45 net10 GND net9 GND sky130_fd_pr__nfet_01v8 L=.6 W=1.5 nf=1 ad='int((nf+1)/2) * W/nf * 0.29' as='int((nf+2)/2) * W/nf * 0.29'
+ pd='2*int((nf+1)/2) * (W/nf + 0.29)' ps='2*int((nf+2)/2) * (W/nf + 0.29)' nrd='0.29 / W' nrs='0.29 / W'
+ sa=0 sb=0 sd=0 mult=1 m=1
XM47 GND net9 net17 GND sky130_fd_pr__nfet_01v8 L=.6 W=1.5 nf=1 ad='int((nf+1)/2) * W/nf * 0.29' as='int((nf+2)/2) * W/nf * 0.29'
+ pd='2*int((nf+1)/2) * (W/nf + 0.29)' ps='2*int((nf+2)/2) * (W/nf + 0.29)' nrd='0.29 / W' nrs='0.29 / W'
+ sa=0 sb=0 sd=0 mult=1 m=1
XM50 net3 V1 net19 GND sky130_fd_pr__nfet_01v8 L=.6 W=1.5 nf=1 ad='int((nf+1)/2) * W/nf * 0.29' as='int((nf+2)/2) * W/nf * 0.29'
+ pd='2*int((nf+1)/2) * (W/nf + 0.29)' ps='2*int((nf+2)/2) * (W/nf + 0.29)' nrd='0.29 / W' nrs='0.29 / W'
+ sa=0 sb=0 sd=0 mult=1 m=1
XMD52 net18 GND net24 GND sky130_fd_pr__nfet_01v8 L=.6 W=1.5 nf=1 ad='int((nf+1)/2) * W/nf * 0.29' as='int((nf+2)/2) * W/nf * 0.29'
+ pd='2*int((nf+1)/2) * (W/nf + 0.29)' ps='2*int((nf+2)/2) * (W/nf + 0.29)' nrd='0.29 / W' nrs='0.29 / W'
+ sa=0 sb=0 sd=0 mult=1 m=1
XM53 net4 V2 net19 GND sky130_fd_pr__nfet_01v8 L=.6 W=1.5 nf=1 ad='int((nf+1)/2) * W/nf * 0.29' as='int((nf+2)/2) * W/nf * 0.29'
+ pd='2*int((nf+1)/2) * (W/nf + 0.29)' ps='2*int((nf+2)/2) * (W/nf + 0.29)' nrd='0.29 / W' nrs='0.29 / W'
+ sa=0 sb=0 sd=0 mult=1 m=1
XM57 net19 net9 GND GND sky130_fd_pr__nfet_01v8 L=.6 W=1.5 nf=1 ad='int((nf+1)/2) * W/nf * 0.29' as='int((nf+2)/2) * W/nf * 0.29'
+ pd='2*int((nf+1)/2) * (W/nf + 0.29)' ps='2*int((nf+2)/2) * (W/nf + 0.29)' nrd='0.29 / W' nrs='0.29 / W'
+ sa=0 sb=0 sd=0 mult=1 m=1
XMD58 net19 GND GND GND sky130_fd_pr__nfet_01v8 L=.6 W=1.5 nf=1 ad='int((nf+1)/2) * W/nf * 0.29' as='int((nf+2)/2) * W/nf * 0.29'
+ pd='2*int((nf+1)/2) * (W/nf + 0.29)' ps='2*int((nf+2)/2) * (W/nf + 0.29)' nrd='0.29 / W' nrs='0.29 / W'
+ sa=0 sb=0 sd=0 mult=1 m=1
XMD59 net2 GND net25 GND sky130_fd_pr__nfet_01v8 L=.6 W=1.5 nf=1 ad='int((nf+1)/2) * W/nf * 0.29' as='int((nf+2)/2) * W/nf * 0.29'
+ pd='2*int((nf+1)/2) * (W/nf + 0.29)' ps='2*int((nf+2)/2) * (W/nf + 0.29)' nrd='0.29 / W' nrs='0.29 / W'
+ sa=0 sb=0 sd=0 mult=1 m=1
XM64 GND net9 net7 GND sky130_fd_pr__nfet_01v8 L=.6 W=1.5 nf=1 ad='int((nf+1)/2) * W/nf * 0.29' as='int((nf+2)/2) * W/nf * 0.29'
+ pd='2*int((nf+1)/2) * (W/nf + 0.29)' ps='2*int((nf+2)/2) * (W/nf + 0.29)' nrd='0.29 / W' nrs='0.29 / W'
+ sa=0 sb=0 sd=0 mult=1 m=1
XMD68 VOUT GND GND GND sky130_fd_pr__nfet_01v8 L=.6 W=1.5 nf=1 ad='int((nf+1)/2) * W/nf * 0.29' as='int((nf+2)/2) * W/nf * 0.29'
+ pd='2*int((nf+1)/2) * (W/nf + 0.29)' ps='2*int((nf+2)/2) * (W/nf + 0.29)' nrd='0.29 / W' nrs='0.29 / W'
+ sa=0 sb=0 sd=0 mult=1 m=1
XM69 GND net9 net6 GND sky130_fd_pr__nfet_01v8 L=.6 W=1.5 nf=1 ad='int((nf+1)/2) * W/nf * 0.29' as='int((nf+2)/2) * W/nf * 0.29'
+ pd='2*int((nf+1)/2) * (W/nf + 0.29)' ps='2*int((nf+2)/2) * (W/nf + 0.29)' nrd='0.29 / W' nrs='0.29 / W'
+ sa=0 sb=0 sd=0 mult=1 m=1
XM70 net7 net18 net18 GND sky130_fd_pr__nfet_01v8 L=.6 W=1.5 nf=1 ad='int((nf+1)/2) * W/nf * 0.29' as='int((nf+2)/2) * W/nf * 0.29'
+ pd='2*int((nf+1)/2) * (W/nf + 0.29)' ps='2*int((nf+2)/2) * (W/nf + 0.29)' nrd='0.29 / W' nrs='0.29 / W'
+ sa=0 sb=0 sd=0 mult=1 m=1
XM71 net6 net18 net2 GND sky130_fd_pr__nfet_01v8 L=.6 W=1.5 nf=1 ad='int((nf+1)/2) * W/nf * 0.29' as='int((nf+2)/2) * W/nf * 0.29'
+ pd='2*int((nf+1)/2) * (W/nf + 0.29)' ps='2*int((nf+2)/2) * (W/nf + 0.29)' nrd='0.29 / W' nrs='0.29 / W'
+ sa=0 sb=0 sd=0 mult=1 m=1
XMD72 VOUT GND GND GND sky130_fd_pr__nfet_01v8 L=.6 W=1.5 nf=1 ad='int((nf+1)/2) * W/nf * 0.29' as='int((nf+2)/2) * W/nf * 0.29'
+ pd='2*int((nf+1)/2) * (W/nf + 0.29)' ps='2*int((nf+2)/2) * (W/nf + 0.29)' nrd='0.29 / W' nrs='0.29 / W'
+ sa=0 sb=0 sd=0 mult=1 m=1
XM73 GND net2 VOUT GND sky130_fd_pr__nfet_01v8 L=.6 W=1.5 nf=1 ad='int((nf+1)/2) * W/nf * 0.29' as='int((nf+2)/2) * W/nf * 0.29'
+ pd='2*int((nf+1)/2) * (W/nf + 0.29)' ps='2*int((nf+2)/2) * (W/nf + 0.29)' nrd='0.29 / W' nrs='0.29 / W'
+ sa=0 sb=0 sd=0 mult=1 m=1
XM74 GND net2 VOUT GND sky130_fd_pr__nfet_01v8 L=.6 W=1.5 nf=1 ad='int((nf+1)/2) * W/nf * 0.29' as='int((nf+2)/2) * W/nf * 0.29'
+ pd='2*int((nf+1)/2) * (W/nf + 0.29)' ps='2*int((nf+2)/2) * (W/nf + 0.29)' nrd='0.29 / W' nrs='0.29 / W'
+ sa=0 sb=0 sd=0 mult=1 m=1
XM75 net21 net10 GND VDD sky130_fd_pr__pfet_01v8 L=.6 W=1.5 nf=1 ad='int((nf+1)/2) * W/nf * 0.29' as='int((nf+2)/2) * W/nf * 0.29'
+ pd='2*int((nf+1)/2) * (W/nf + 0.29)' ps='2*int((nf+2)/2) * (W/nf + 0.29)' nrd='0.29 / W' nrs='0.29 / W'
+ sa=0 sb=0 sd=0 mult=1 m=1
XM76 net10 net10 net4 VDD sky130_fd_pr__pfet_01v8 L=.6 W=1.5 nf=1 ad='int((nf+1)/2) * W/nf * 0.29' as='int((nf+2)/2) * W/nf * 0.29'
+ pd='2*int((nf+1)/2) * (W/nf + 0.29)' ps='2*int((nf+2)/2) * (W/nf + 0.29)' nrd='0.29 / W' nrs='0.29 / W'
+ sa=0 sb=0 sd=0 mult=1 m=1
XM77 net17 net9 VDD GND sky130_fd_pr__nfet_01v8 L=.6 W=1.5 nf=1 ad='int((nf+1)/2) * W/nf * 0.29' as='int((nf+2)/2) * W/nf * 0.29'
+ pd='2*int((nf+1)/2) * (W/nf + 0.29)' ps='2*int((nf+2)/2) * (W/nf + 0.29)' nrd='0.29 / W' nrs='0.29 / W'
+ sa=0 sb=0 sd=0 mult=1 m=1
XM78 net9 net9 net7 GND sky130_fd_pr__nfet_01v8 L=.6 W=1.5 nf=1 ad='int((nf+1)/2) * W/nf * 0.29' as='int((nf+2)/2) * W/nf * 0.29'
+ pd='2*int((nf+1)/2) * (W/nf + 0.29)' ps='2*int((nf+2)/2) * (W/nf + 0.29)' nrd='0.29 / W' nrs='0.29 / W'
+ sa=0 sb=0 sd=0 mult=1 m=1
XMD79 VDD GND GND GND sky130_fd_pr__nfet_01v8 L=.6 W=1.5 nf=1 ad='int((nf+1)/2) * W/nf * 0.29' as='int((nf+2)/2) * W/nf * 0.29'
+ pd='2*int((nf+1)/2) * (W/nf + 0.29)' ps='2*int((nf+2)/2) * (W/nf + 0.29)' nrd='0.29 / W' nrs='0.29 / W'
+ sa=0 sb=0 sd=0 mult=1 m=1
XMD80 net7 GND GND GND sky130_fd_pr__nfet_01v8 L=.6 W=1.5 nf=1 ad='int((nf+1)/2) * W/nf * 0.29' as='int((nf+2)/2) * W/nf * 0.29'
+ pd='2*int((nf+1)/2) * (W/nf + 0.29)' ps='2*int((nf+2)/2) * (W/nf + 0.29)' nrd='0.29 / W' nrs='0.29 / W'
+ sa=0 sb=0 sd=0 mult=1 m=1
XMD81 GND VDD VDD VDD sky130_fd_pr__pfet_01v8 L=.6 W=1.5 nf=1 ad='int((nf+1)/2) * W/nf * 0.29' as='int((nf+2)/2) * W/nf * 0.29'
+ pd='2*int((nf+1)/2) * (W/nf + 0.29)' ps='2*int((nf+2)/2) * (W/nf + 0.29)' nrd='0.29 / W' nrs='0.29 / W'
+ sa=0 sb=0 sd=0 mult=1 m=1
XMD82 net4 VDD VDD VDD sky130_fd_pr__pfet_01v8 L=.6 W=1.5 nf=1 ad='int((nf+1)/2) * W/nf * 0.29' as='int((nf+2)/2) * W/nf * 0.29'
+ pd='2*int((nf+1)/2) * (W/nf + 0.29)' ps='2*int((nf+2)/2) * (W/nf + 0.29)' nrd='0.29 / W' nrs='0.29 / W'
+ sa=0 sb=0 sd=0 mult=1 m=1
XMD83 net24 GND net3 GND sky130_fd_pr__nfet_01v8 L=.6 W=1.5 nf=1 ad='int((nf+1)/2) * W/nf * 0.29' as='int((nf+2)/2) * W/nf * 0.29'
+ pd='2*int((nf+1)/2) * (W/nf + 0.29)' ps='2*int((nf+2)/2) * (W/nf + 0.29)' nrd='0.29 / W' nrs='0.29 / W'
+ sa=0 sb=0 sd=0 mult=1 m=1
XMD84 net25 GND net4 GND sky130_fd_pr__nfet_01v8 L=.6 W=1.5 nf=1 ad='int((nf+1)/2) * W/nf * 0.29' as='int((nf+2)/2) * W/nf * 0.29'
+ pd='2*int((nf+1)/2) * (W/nf + 0.29)' ps='2*int((nf+2)/2) * (W/nf + 0.29)' nrd='0.29 / W' nrs='0.29 / W'
+ sa=0 sb=0 sd=0 mult=1 m=1
XMD85 net22 VDD net6 VDD sky130_fd_pr__pfet_01v8 L=.6 W=1.5 nf=1 ad='int((nf+1)/2) * W/nf * 0.29' as='int((nf+2)/2) * W/nf * 0.29'
+ pd='2*int((nf+1)/2) * (W/nf + 0.29)' ps='2*int((nf+2)/2) * (W/nf + 0.29)' nrd='0.29 / W' nrs='0.29 / W'
+ sa=0 sb=0 sd=0 mult=1 m=1
XMD86 net23 VDD net7 VDD sky130_fd_pr__pfet_01v8 L=.6 W=1.5 nf=1 ad='int((nf+1)/2) * W/nf * 0.29' as='int((nf+2)/2) * W/nf * 0.29'
+ pd='2*int((nf+1)/2) * (W/nf + 0.29)' ps='2*int((nf+2)/2) * (W/nf + 0.29)' nrd='0.29 / W' nrs='0.29 / W'
+ sa=0 sb=0 sd=0 mult=1 m=1
XC1 net2 VOUT sky130_fd_pr__cap_mim_m3_1 W=20 L=12 MF=1 m=1
.ends

.GLOBAL GND
.GLOBAL VDD
.end
